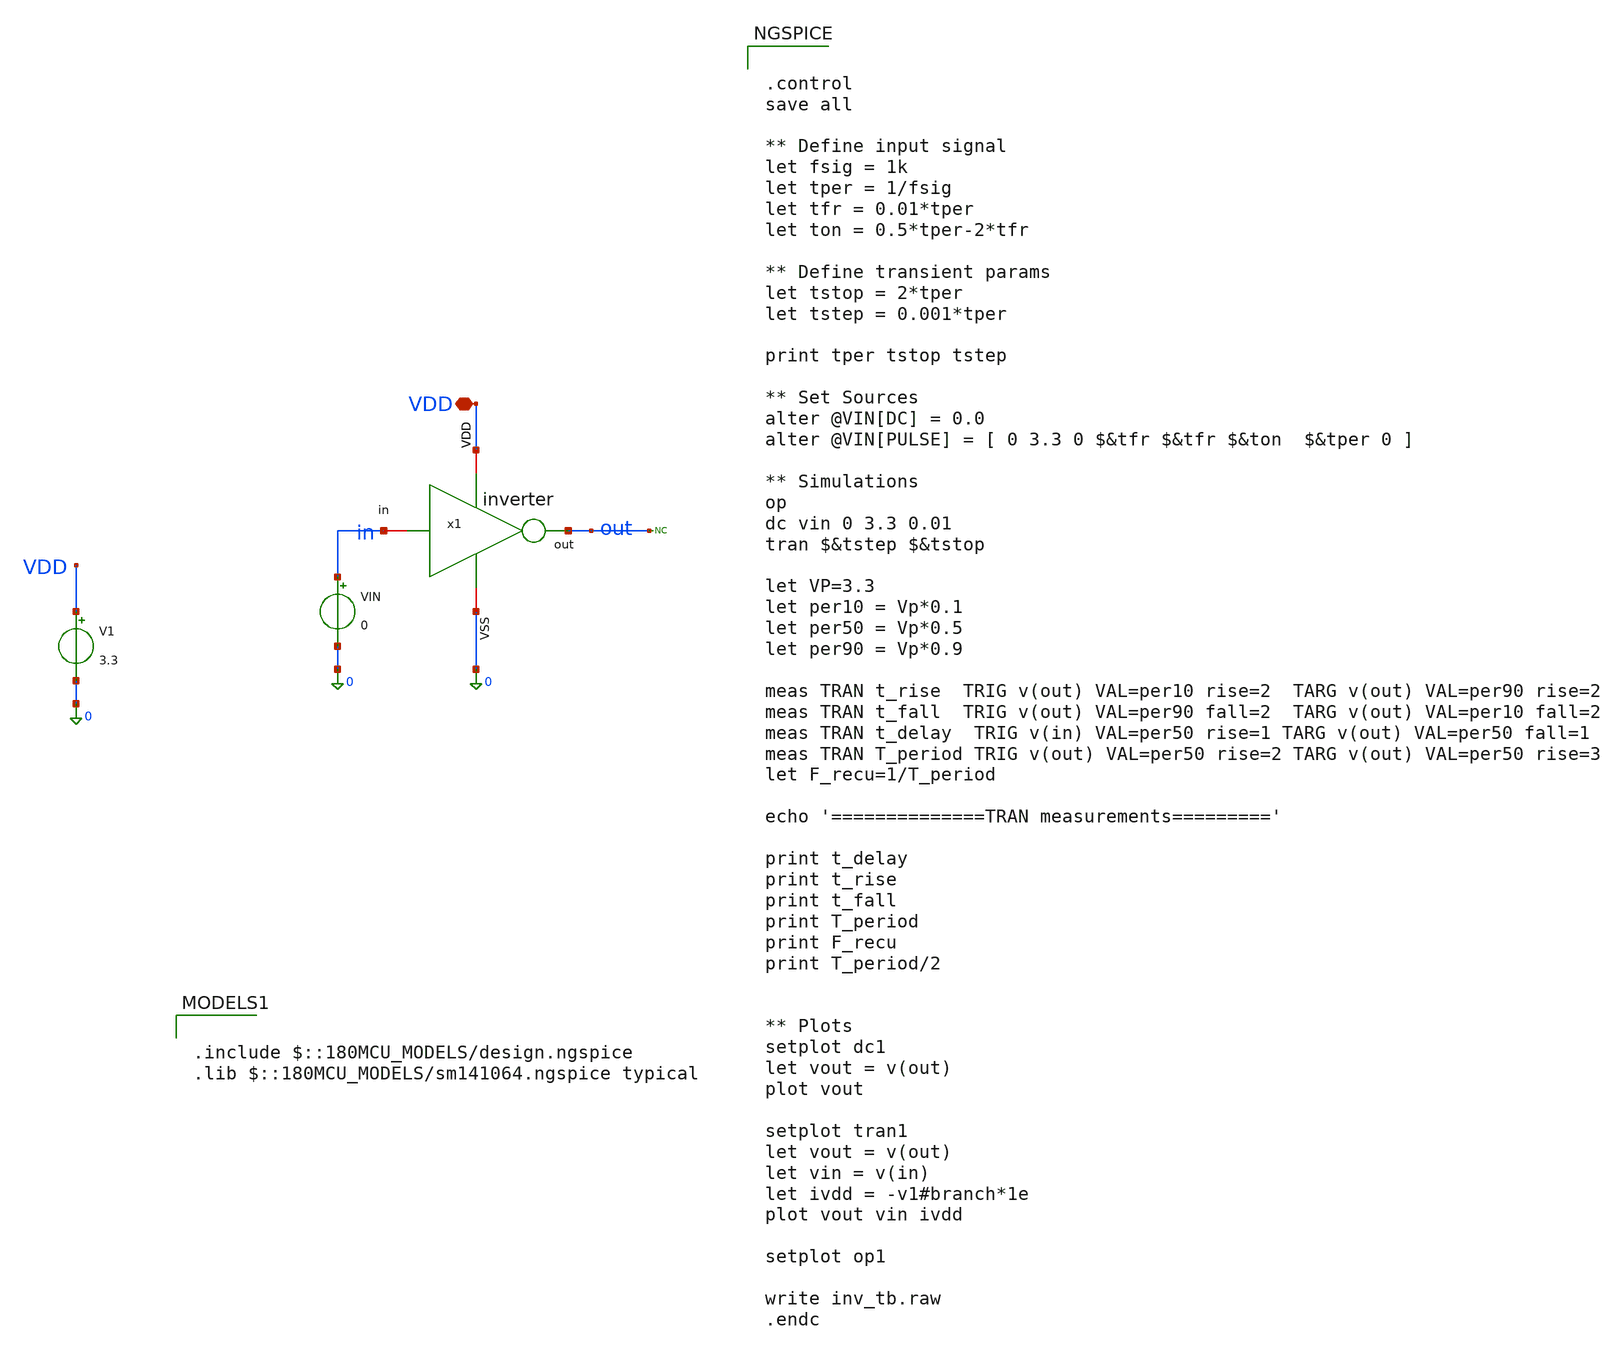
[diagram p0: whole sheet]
** sch_path: designs/sar_adc/digital/inverter/xschem/inv_tb.sch
**.subckt inv_tb VDD
*.iopin VDD
V1 VDD 0 3.3
VIN in 0 0
x1 VDD in out 0 inverter
* noconn out
**** begin user architecture code


.control
save all

** Define input signal
let fsig = 1k
let tper = 1/fsig
let tfr = 0.01*tper
let ton = 0.5*tper-2*tfr

** Define transient params
let tstop = 2*tper
let tstep = 0.001*tper

print tper tstop tstep

** Set Sources
alter @VIN[DC] = 0.0
alter @VIN[PULSE] = [ 0 3.3 0 $&tfr $&tfr $&ton  $&tper 0 ]

** Simulations
op
dc vin 0 3.3 0.01
tran $&tstep $&tstop

let VP=3.3
let per10 = Vp*0.1
let per50 = Vp*0.5
let per90 = Vp*0.9

meas TRAN t_rise  TRIG v(out) VAL=per10 rise=2  TARG v(out) VAL=per90 rise=2
meas TRAN t_fall  TRIG v(out) VAL=per90 fall=2  TARG v(out) VAL=per10 fall=2
meas TRAN t_delay  TRIG v(in) VAL=per50 rise=1 TARG v(out) VAL=per50 fall=1
meas TRAN T_period TRIG v(out) VAL=per50 rise=2 TARG v(out) VAL=per50 rise=3
let F_recu=1/T_period

echo '==============TRAN measurements========='

print t_delay
print t_rise
print t_fall
print T_period
print F_recu
print T_period/2


** Plots
setplot dc1
let vout = v(out)
plot vout

setplot tran1
let vout = v(out)
let vin = v(in)
let ivdd = -v1#branch*1e
plot vout vin ivdd

setplot op1

write inv_tb.raw
.endc



.include $::180MCU_MODELS/design.ngspice
.lib $::180MCU_MODELS/sm141064.ngspice typical

**** end user architecture code
**.ends

* expanding   symbol:  designs/sar_adc/digital/inverter/xschem/inverter.sym # of pins=6
** sym_path: designs/sar_adc/digital/inverter/xschem/inverter.sym
** sch_path: designs/sar_adc/digital/inverter/xschem/inverter.sch
.subckt inverter VDD in out VSS
*.opin out
*.iopin in
*.iopin VDD
*.iopin VSS
XM1 out in VSS VSS nfet_03v3 L=0.28u W=0.22u nf=1 ad='int((nf+1)/2) * W/nf * 0.18u' as='int((nf+2)/2) * W/nf * 0.18u'
+ pd='2*int((nf+1)/2) * (W/nf + 0.18u)' ps='2*int((nf+2)/2) * (W/nf + 0.18u)' nrd='0.18u / W' nrs='0.18u / W'
+ sa=0 sb=0 sd=0 m=1
XM2 out in VDD VDD pfet_03v3 L=0.28u W=0.22u nf=1 ad='int((nf+1)/2) * W/nf * 0.18u' as='int((nf+2)/2) * W/nf * 0.18u'
+ pd='2*int((nf+1)/2) * (W/nf + 0.18u)' ps='2*int((nf+2)/2) * (W/nf + 0.18u)' nrd='0.18u / W' nrs='0.18u / W'
+ sa=0 sb=0 sd=0 m=1
.ends

.end
